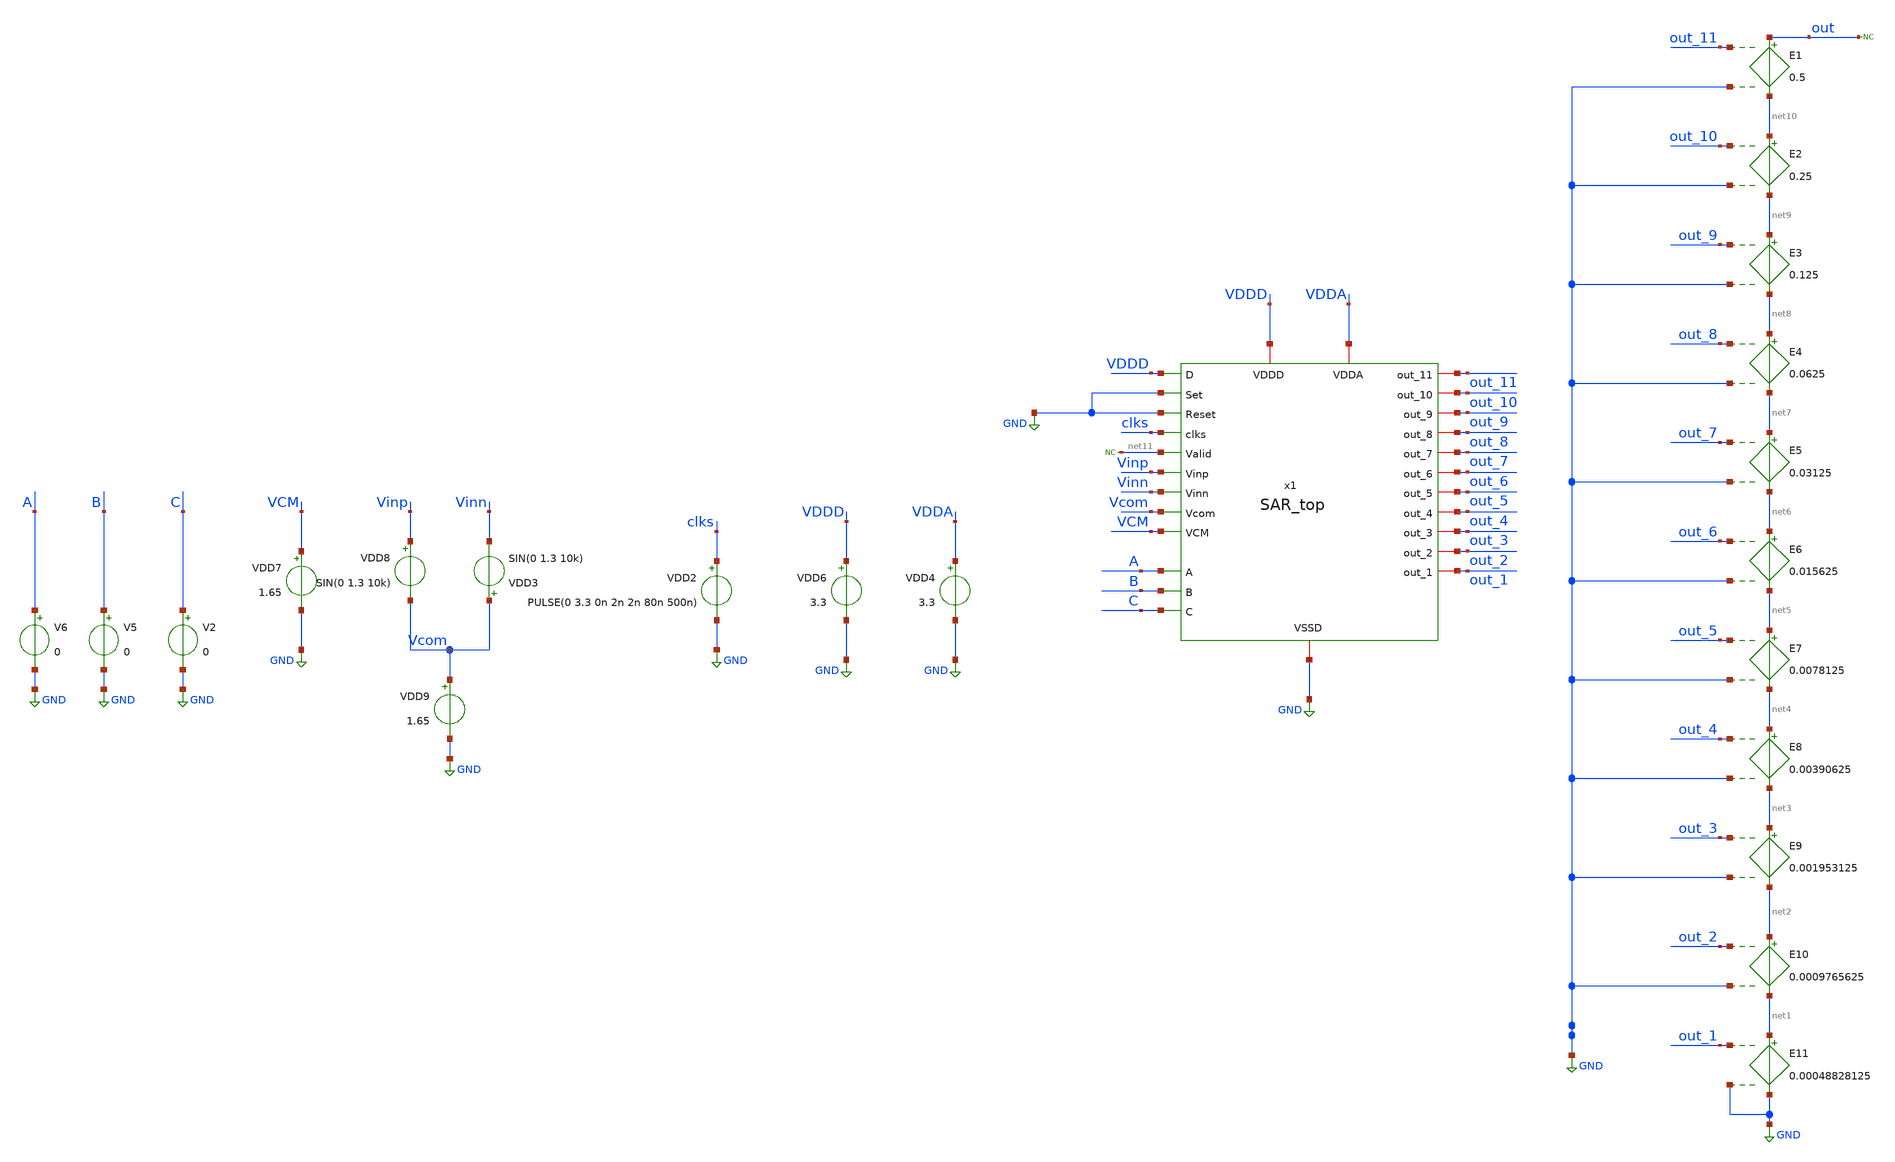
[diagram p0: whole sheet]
** sch_path: SAR_ADC/SAR_top/xschem/SAR_top_tb.sch
**.subckt SAR_top_tb
x1 out_11 GND GND out_10 out_9 VDDD out_8 VDDA GND out_7 clks out_6 Vinp Vinn out_5 Vcom out_4 net11
+ out_3 A B out_2 C VDDD out_1 VCM SAR_top
VDD4 VDDA GND 3.3
VDD6 VDDD GND 3.3
E1 out net10 out_11 GND 0.5
E2 net10 net9 out_10 GND 0.25
E3 net9 net8 out_9 GND 0.125
E4 net8 net7 out_8 GND 0.0625
E5 net7 net6 out_7 GND 0.03125
E6 net6 net5 out_6 GND 0.015625
E7 net5 net4 out_5 GND 0.0078125
E8 net4 net3 out_4 GND 0.00390625
E9 net3 net2 out_3 GND 0.001953125
E10 net2 net1 out_2 GND 0.0009765625
E11 net1 GND out_1 GND 0.00048828125
* noconn out
VDD2 clks GND PULSE(0 3.3 0n 2n 2n 80n 500n)
* noconn #net11
VDD3 Vcom Vinn SIN(0 1.3 10k)
VDD8 Vinp Vcom SIN(0 1.3 10k)
VDD9 Vcom GND 1.65
VDD7 VCM GND 1.65
V2 C GND 0
V5 B GND 0
V6 A GND 0
**** begin user architecture code



*Parameters

.options TEMP = 50
.lib /home/gf180/Documents/gf180/pdk/gf180mcuD/libs.tech/ngspice/sm141064.ngspice typical
.lib /home/gf180/Documents/gf180/pdk/gf180mcuD/libs.tech/ngspice/sm141064.ngspice cap_mim

.lib /home/gf180/Documents/gf180/pdk/gf180mcuD/libs.tech/ngspice/sm141064.ngspice mimcap_statistical
.include /home/gf180/Documents/gf180/pdk/gf180mcuD/libs.tech/ngspice/design.ngspice

*Data to save
.save v(Vinp)
.save v(Vinn)
*.save v(Valid)
*.save v(CK11)
*.save v(CK10)
*.save v(CK9)
*.save v(CK8)
*.save v(CK7)
*.save v(CK6)
*.save v(CK5)
*.save v(CK4)
*.save v(CK3)
*.save v(CK2)
*.save v(CK1)
*.save v(Bit_10)
*.save v(Bit_10_n)
*.save v(Bit_9)
*.save v(Bit_9_n)
*.save v(Bit_8)
*.save v(Bit_8_n)
*.save v(Bit_7)
*.save v(Bit_7_n)
*.save v(Bit_6)
*.save v(Bit_6_n)
*.save v(Bit_5)
*.save v(Bit_5_n)
*.save v(Bit_4)
*.save v(Bit_4_n)
*.save v(Bit_3)
*.save v(Bit_3_n)
*.save v(Bit_2)
*.save v(Bit_2_n)
*.save v(Bit_1)
*.save v(Bit_1_n)
*.save v(vocp)
*.save v(vocn)
.save v(out)

* Simulation
.control
tran 500n 100u
*setplot dc1
*let vout_diff = VDP - VDN
let vin_diff = Vinp - Vinn
*plot v(Bit_10_n)+48 v(Bit_10)+48 v(Bit_9_n)+44 v(Bit_9)+44 v(Bit_8_n)+40 v(Bit_8)+40 v(Bit_7_n)+36
*+ v(Bit_7)+36 v(Bit_6_n)+32 v(Bit_6)+32 v(Bit_5_n)+28 v(Bit_5)+28 v(Bit_4_n)+24 v(Bit_4)+24 v(Bit_3_n)+20
*+ v(Bit_3)+20 v(Bit_2_n)+16 v(Bit_2)+16 v(Bit_1_n)+12 v(Bit_1)+12 v(clks)+8 v(Valid)+4 v(vin_diff) v(vout_diff)
*plot v(clks)+8 v(Vinp)+4 v(VDP)+4 v(Vinn) v(VDN)
*set filetype=ascii
*plot v(clks)+12 v(Valid)+8 v(vin_diff)+4 v(vout_diff)+4 v(Vinp) v(out)
plot (vin_diff) v(out)

*setplot dc2
*plot v(clks)+8 v(Vinp)+4 v(VDP)

*setplot dc3
*plot v(clkc)+20 v(VDP)+16 v(VDN)+12 v(vocp)+8 v(vocn)+4 v(Valid)

*setplot dc4
*plot v(Valid)+48 v(clks)+44 v(CK11)+40 v(CK10)+36 v(CK9)+32 v(CK8)+28 v(CK7)+24 v(CK6)+20 v(CK5)+16
*+ v(CK4)+12 v(CK3)+8 v(CK2)+4 v(CK1)

*setplot dc1
*plot v(VDP)+20 v(VDN)+20 v(clkc)+16 v(x5.aN)+12 v(x5.aP)+8 v(x5.dP)+4 v(x5.dN)

set filetype = ascii
write SAR_top_tb_dc.raw

reset
unset filetype
op
save all
write SAR_top_tb.raw


.endc
.end


**** end user architecture code
**.ends
.GLOBAL GND
.end
